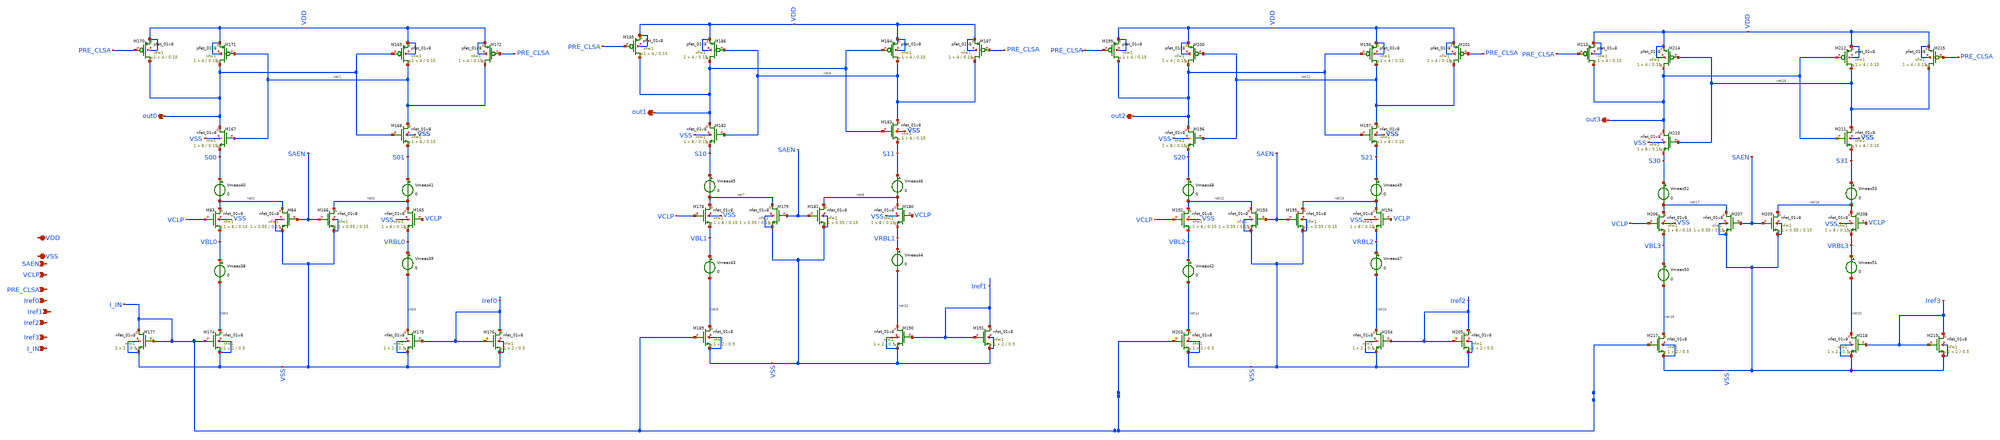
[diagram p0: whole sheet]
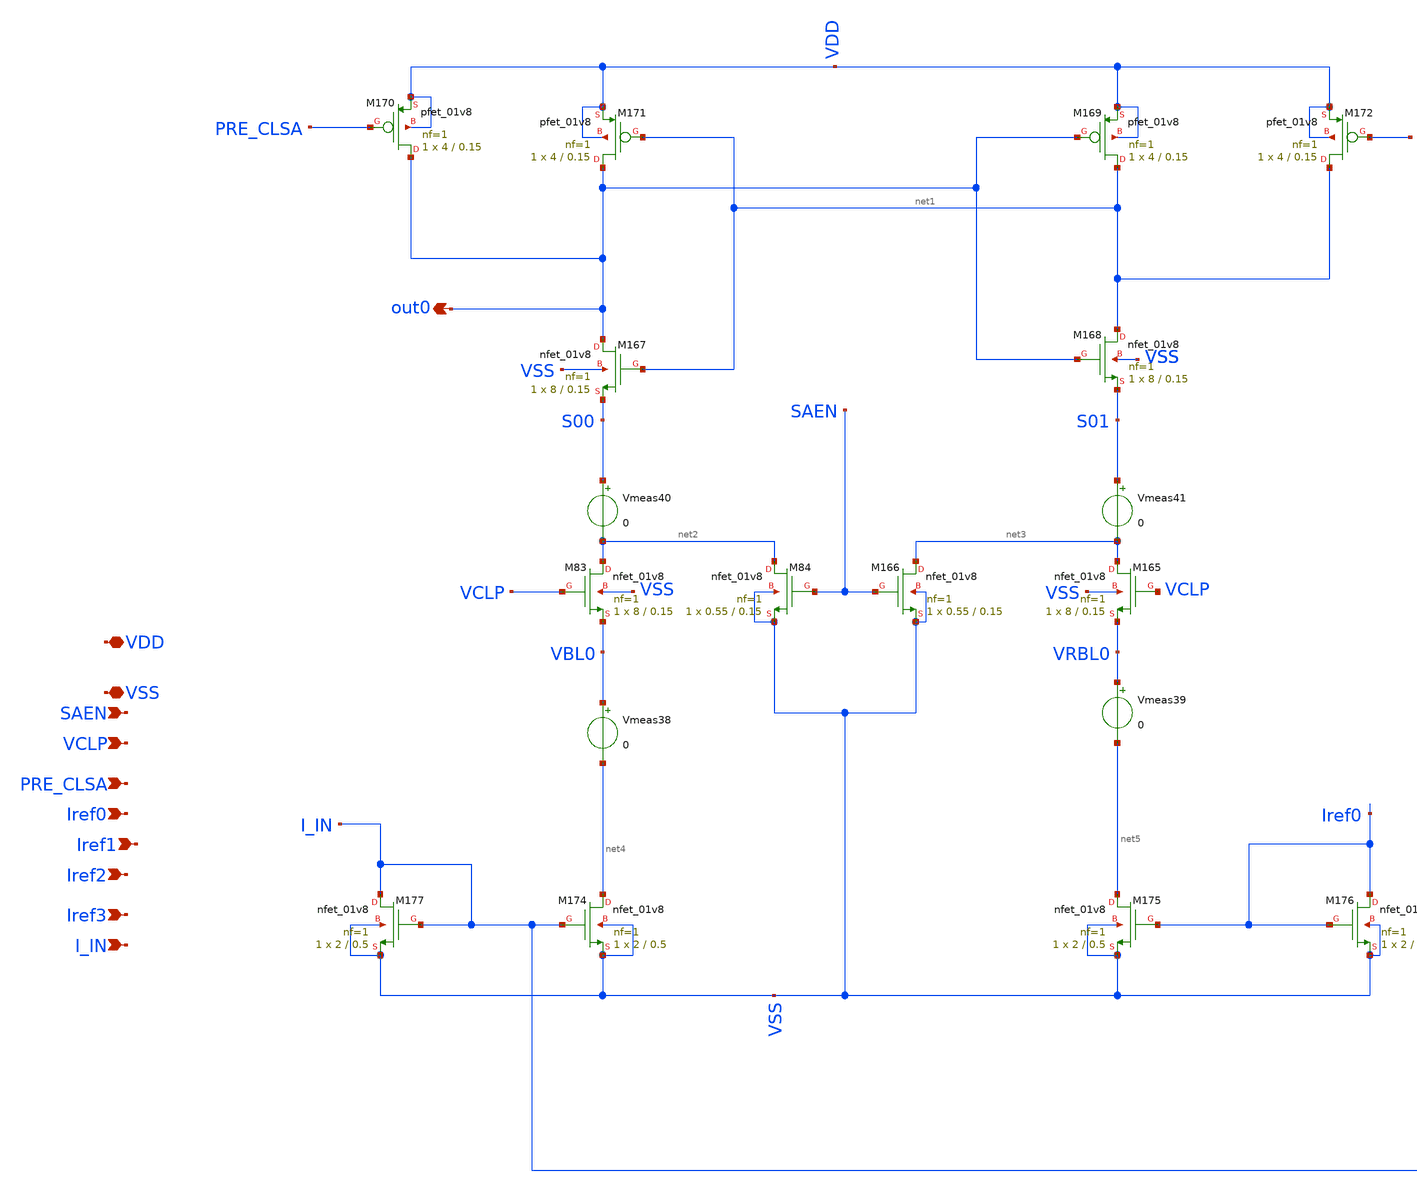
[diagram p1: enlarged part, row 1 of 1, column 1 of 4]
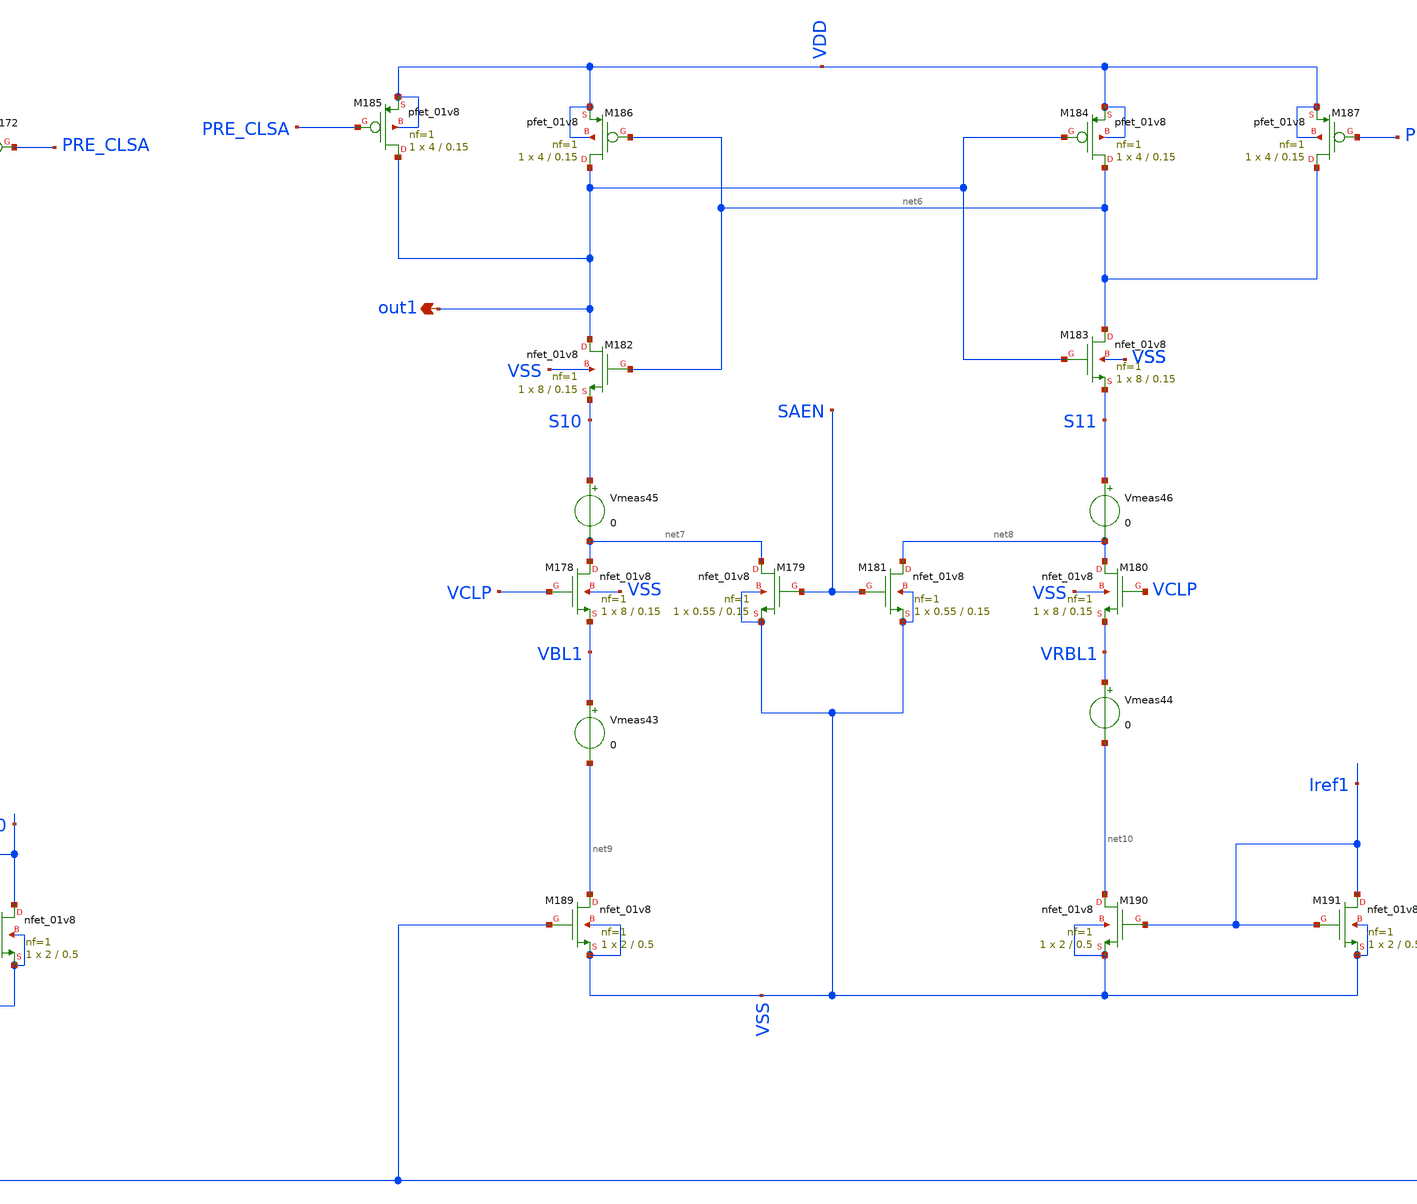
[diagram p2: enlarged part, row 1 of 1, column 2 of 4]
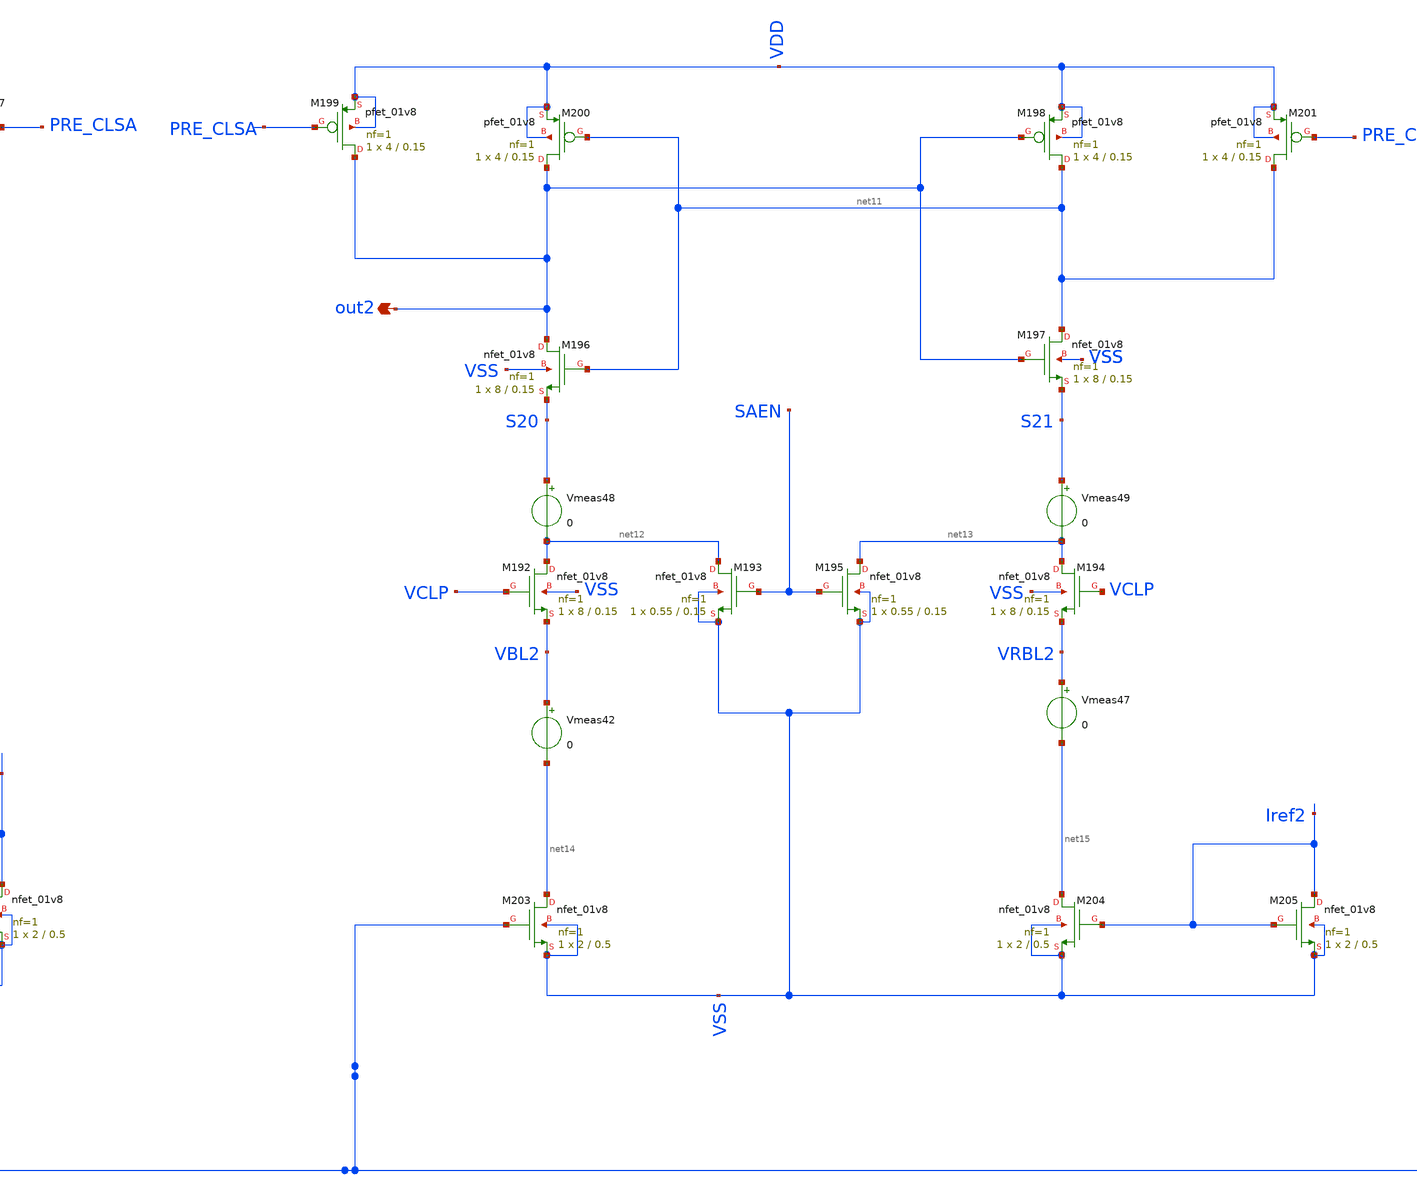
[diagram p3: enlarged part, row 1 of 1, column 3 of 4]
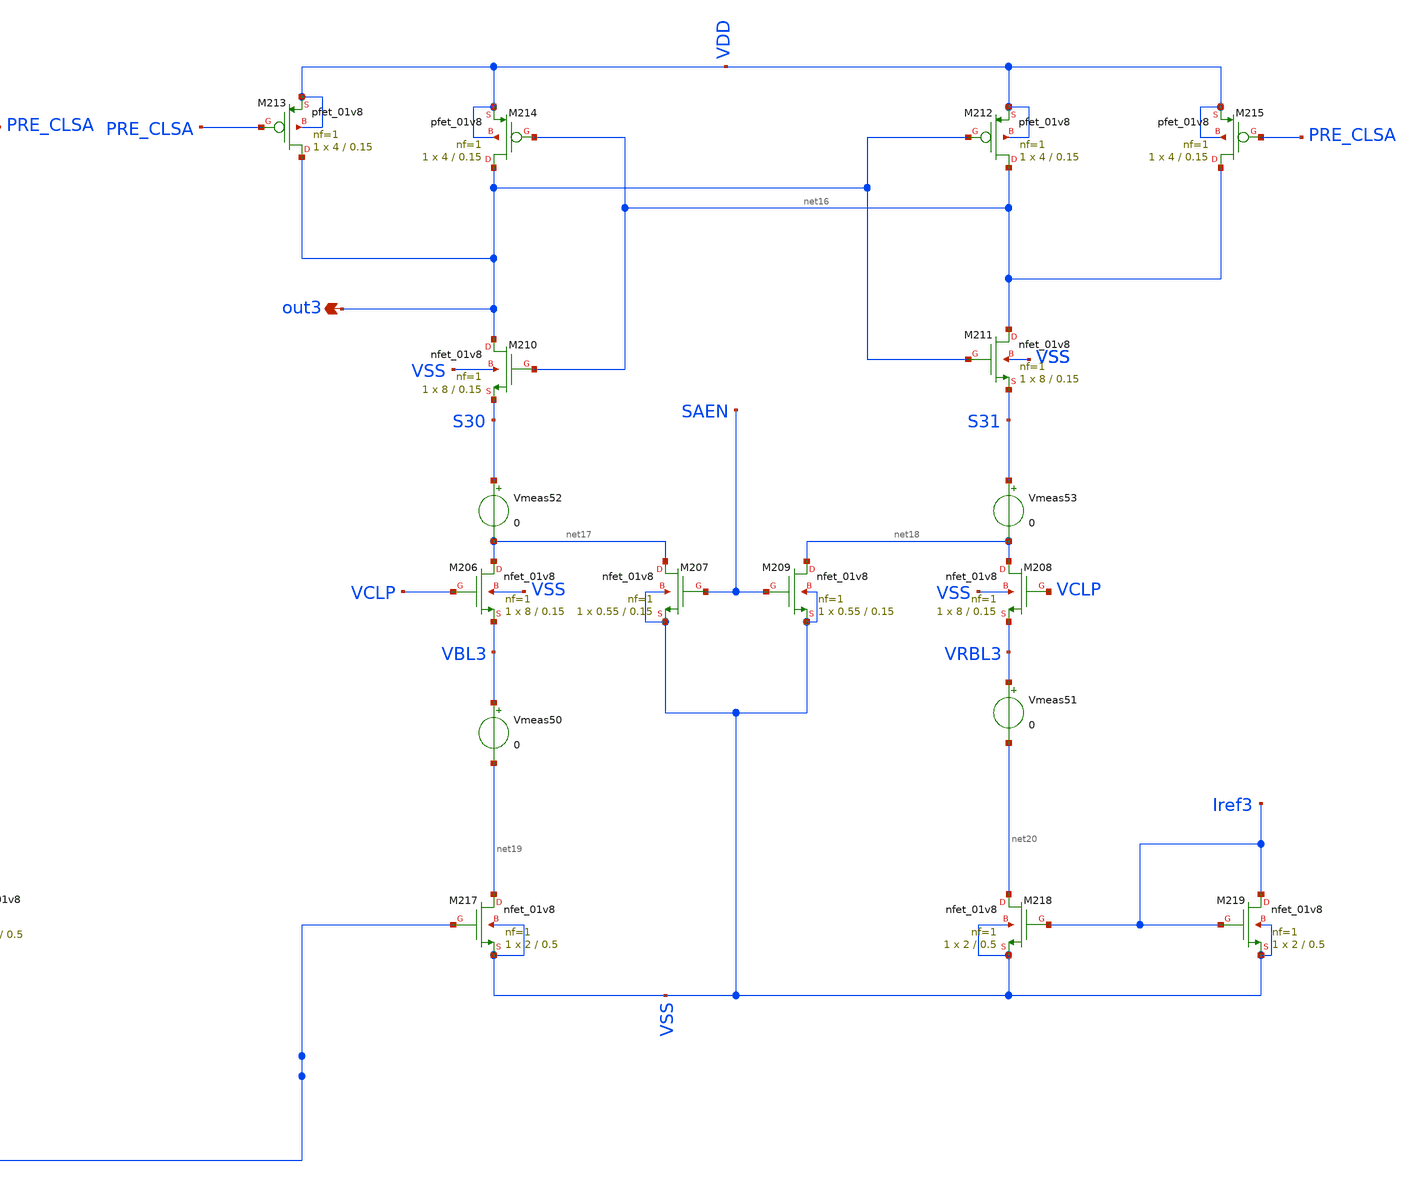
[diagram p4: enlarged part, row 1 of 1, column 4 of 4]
** sch_path: xschem/Integrated_bitcell/ADC_CLSA_4.sch
**.subckt ADC_CLSA_4 out0 out1 out2 out3 VDD VSS VCLP PRE_CLSA Iref0 Iref1 Iref2 Iref3 SAEN I_IN
*.opin out0
*.opin out1
*.opin out2
*.opin out3
*.iopin VDD
*.iopin VSS
*.ipin VCLP
*.ipin PRE_CLSA
*.ipin Iref0
*.ipin Iref1
*.ipin Iref2
*.ipin Iref3
*.ipin SAEN
*.ipin I_IN
XM83 net2 VCLP VBL0 VSS sky130_fd_pr__nfet_01v8 L=0.15 W=8 nf=1 ad='int((nf+1)/2) * W/nf * 0.29' as='int((nf+2)/2) * W/nf * 0.29'
+ pd='2*int((nf+1)/2) * (W/nf + 0.29)' ps='2*int((nf+2)/2) * (W/nf + 0.29)' nrd='0.29 / W' nrs='0.29 / W'
+ sa=0 sb=0 sd=0 mult=1 m=1
XM84 net2 SAEN VSS VSS sky130_fd_pr__nfet_01v8 L=0.15 W=0.55 nf=1 ad='int((nf+1)/2) * W/nf * 0.29' as='int((nf+2)/2) * W/nf * 0.29'
+ pd='2*int((nf+1)/2) * (W/nf + 0.29)' ps='2*int((nf+2)/2) * (W/nf + 0.29)' nrd='0.29 / W' nrs='0.29 / W'
+ sa=0 sb=0 sd=0 mult=1 m=1
XM165 net3 VCLP VRBL0 VSS sky130_fd_pr__nfet_01v8 L=0.15 W=8 nf=1 ad='int((nf+1)/2) * W/nf * 0.29' as='int((nf+2)/2) * W/nf * 0.29'
+ pd='2*int((nf+1)/2) * (W/nf + 0.29)' ps='2*int((nf+2)/2) * (W/nf + 0.29)' nrd='0.29 / W' nrs='0.29 / W'
+ sa=0 sb=0 sd=0 mult=1 m=1
XM166 net3 SAEN VSS VSS sky130_fd_pr__nfet_01v8 L=0.15 W=0.55 nf=1 ad='int((nf+1)/2) * W/nf * 0.29' as='int((nf+2)/2) * W/nf * 0.29'
+ pd='2*int((nf+1)/2) * (W/nf + 0.29)' ps='2*int((nf+2)/2) * (W/nf + 0.29)' nrd='0.29 / W' nrs='0.29 / W'
+ sa=0 sb=0 sd=0 mult=1 m=1
XM167 out0 net1 S00 VSS sky130_fd_pr__nfet_01v8 L=0.15 W=8 nf=1 ad='int((nf+1)/2) * W/nf * 0.29' as='int((nf+2)/2) * W/nf * 0.29'
+ pd='2*int((nf+1)/2) * (W/nf + 0.29)' ps='2*int((nf+2)/2) * (W/nf + 0.29)' nrd='0.29 / W' nrs='0.29 / W'
+ sa=0 sb=0 sd=0 mult=1 m=1
XM168 net1 out0 S01 VSS sky130_fd_pr__nfet_01v8 L=0.15 W=8 nf=1 ad='int((nf+1)/2) * W/nf * 0.29' as='int((nf+2)/2) * W/nf * 0.29'
+ pd='2*int((nf+1)/2) * (W/nf + 0.29)' ps='2*int((nf+2)/2) * (W/nf + 0.29)' nrd='0.29 / W' nrs='0.29 / W'
+ sa=0 sb=0 sd=0 mult=1 m=1
XM169 net1 out0 VDD VDD sky130_fd_pr__pfet_01v8 L=0.15 W=4 nf=1 ad='int((nf+1)/2) * W/nf * 0.29' as='int((nf+2)/2) * W/nf * 0.29'
+ pd='2*int((nf+1)/2) * (W/nf + 0.29)' ps='2*int((nf+2)/2) * (W/nf + 0.29)' nrd='0.29 / W' nrs='0.29 / W'
+ sa=0 sb=0 sd=0 mult=1 m=1
XM170 out0 PRE_CLSA VDD VDD sky130_fd_pr__pfet_01v8 L=0.15 W=4 nf=1 ad='int((nf+1)/2) * W/nf * 0.29'
+ as='int((nf+2)/2) * W/nf * 0.29' pd='2*int((nf+1)/2) * (W/nf + 0.29)' ps='2*int((nf+2)/2) * (W/nf + 0.29)'
+ nrd='0.29 / W' nrs='0.29 / W' sa=0 sb=0 sd=0 mult=1 m=1
XM171 out0 net1 VDD VDD sky130_fd_pr__pfet_01v8 L=0.15 W=4 nf=1 ad='int((nf+1)/2) * W/nf * 0.29' as='int((nf+2)/2) * W/nf * 0.29'
+ pd='2*int((nf+1)/2) * (W/nf + 0.29)' ps='2*int((nf+2)/2) * (W/nf + 0.29)' nrd='0.29 / W' nrs='0.29 / W'
+ sa=0 sb=0 sd=0 mult=1 m=1
XM172 net1 PRE_CLSA VDD VDD sky130_fd_pr__pfet_01v8 L=0.15 W=4 nf=1 ad='int((nf+1)/2) * W/nf * 0.29'
+ as='int((nf+2)/2) * W/nf * 0.29' pd='2*int((nf+1)/2) * (W/nf + 0.29)' ps='2*int((nf+2)/2) * (W/nf + 0.29)'
+ nrd='0.29 / W' nrs='0.29 / W' sa=0 sb=0 sd=0 mult=1 m=1
Vmeas38 VBL0 net4 0
Vmeas39 VRBL0 net5 0
XM174 net4 I_IN VSS VSS sky130_fd_pr__nfet_01v8 L=0.5 W=2 nf=1 ad='int((nf+1)/2) * W/nf * 0.29' as='int((nf+2)/2) * W/nf * 0.29'
+ pd='2*int((nf+1)/2) * (W/nf + 0.29)' ps='2*int((nf+2)/2) * (W/nf + 0.29)' nrd='0.29 / W' nrs='0.29 / W'
+ sa=0 sb=0 sd=0 mult=1 m=1
XM175 net5 Iref0 VSS VSS sky130_fd_pr__nfet_01v8 L=0.5 W=2 nf=1 ad='int((nf+1)/2) * W/nf * 0.29' as='int((nf+2)/2) * W/nf * 0.29'
+ pd='2*int((nf+1)/2) * (W/nf + 0.29)' ps='2*int((nf+2)/2) * (W/nf + 0.29)' nrd='0.29 / W' nrs='0.29 / W'
+ sa=0 sb=0 sd=0 mult=1 m=1
XM176 Iref0 Iref0 VSS VSS sky130_fd_pr__nfet_01v8 L=0.5 W=2 nf=1 ad='int((nf+1)/2) * W/nf * 0.29' as='int((nf+2)/2) * W/nf * 0.29'
+ pd='2*int((nf+1)/2) * (W/nf + 0.29)' ps='2*int((nf+2)/2) * (W/nf + 0.29)' nrd='0.29 / W' nrs='0.29 / W'
+ sa=0 sb=0 sd=0 mult=1 m=1
XM177 I_IN I_IN VSS VSS sky130_fd_pr__nfet_01v8 L=0.5 W=2 nf=1 ad='int((nf+1)/2) * W/nf * 0.29' as='int((nf+2)/2) * W/nf * 0.29'
+ pd='2*int((nf+1)/2) * (W/nf + 0.29)' ps='2*int((nf+2)/2) * (W/nf + 0.29)' nrd='0.29 / W' nrs='0.29 / W'
+ sa=0 sb=0 sd=0 mult=1 m=1
Vmeas40 S00 net2 0
Vmeas41 S01 net3 0
XM178 net7 VCLP VBL1 VSS sky130_fd_pr__nfet_01v8 L=0.15 W=8 nf=1 ad='int((nf+1)/2) * W/nf * 0.29' as='int((nf+2)/2) * W/nf * 0.29'
+ pd='2*int((nf+1)/2) * (W/nf + 0.29)' ps='2*int((nf+2)/2) * (W/nf + 0.29)' nrd='0.29 / W' nrs='0.29 / W'
+ sa=0 sb=0 sd=0 mult=1 m=1
XM179 net7 SAEN VSS VSS sky130_fd_pr__nfet_01v8 L=0.15 W=0.55 nf=1 ad='int((nf+1)/2) * W/nf * 0.29' as='int((nf+2)/2) * W/nf * 0.29'
+ pd='2*int((nf+1)/2) * (W/nf + 0.29)' ps='2*int((nf+2)/2) * (W/nf + 0.29)' nrd='0.29 / W' nrs='0.29 / W'
+ sa=0 sb=0 sd=0 mult=1 m=1
XM180 net8 VCLP VRBL1 VSS sky130_fd_pr__nfet_01v8 L=0.15 W=8 nf=1 ad='int((nf+1)/2) * W/nf * 0.29' as='int((nf+2)/2) * W/nf * 0.29'
+ pd='2*int((nf+1)/2) * (W/nf + 0.29)' ps='2*int((nf+2)/2) * (W/nf + 0.29)' nrd='0.29 / W' nrs='0.29 / W'
+ sa=0 sb=0 sd=0 mult=1 m=1
XM181 net8 SAEN VSS VSS sky130_fd_pr__nfet_01v8 L=0.15 W=0.55 nf=1 ad='int((nf+1)/2) * W/nf * 0.29' as='int((nf+2)/2) * W/nf * 0.29'
+ pd='2*int((nf+1)/2) * (W/nf + 0.29)' ps='2*int((nf+2)/2) * (W/nf + 0.29)' nrd='0.29 / W' nrs='0.29 / W'
+ sa=0 sb=0 sd=0 mult=1 m=1
XM182 out1 net6 S10 VSS sky130_fd_pr__nfet_01v8 L=0.15 W=8 nf=1 ad='int((nf+1)/2) * W/nf * 0.29' as='int((nf+2)/2) * W/nf * 0.29'
+ pd='2*int((nf+1)/2) * (W/nf + 0.29)' ps='2*int((nf+2)/2) * (W/nf + 0.29)' nrd='0.29 / W' nrs='0.29 / W'
+ sa=0 sb=0 sd=0 mult=1 m=1
XM183 net6 out1 S11 VSS sky130_fd_pr__nfet_01v8 L=0.15 W=8 nf=1 ad='int((nf+1)/2) * W/nf * 0.29' as='int((nf+2)/2) * W/nf * 0.29'
+ pd='2*int((nf+1)/2) * (W/nf + 0.29)' ps='2*int((nf+2)/2) * (W/nf + 0.29)' nrd='0.29 / W' nrs='0.29 / W'
+ sa=0 sb=0 sd=0 mult=1 m=1
XM184 net6 out1 VDD VDD sky130_fd_pr__pfet_01v8 L=0.15 W=4 nf=1 ad='int((nf+1)/2) * W/nf * 0.29' as='int((nf+2)/2) * W/nf * 0.29'
+ pd='2*int((nf+1)/2) * (W/nf + 0.29)' ps='2*int((nf+2)/2) * (W/nf + 0.29)' nrd='0.29 / W' nrs='0.29 / W'
+ sa=0 sb=0 sd=0 mult=1 m=1
XM185 out1 PRE_CLSA VDD VDD sky130_fd_pr__pfet_01v8 L=0.15 W=4 nf=1 ad='int((nf+1)/2) * W/nf * 0.29'
+ as='int((nf+2)/2) * W/nf * 0.29' pd='2*int((nf+1)/2) * (W/nf + 0.29)' ps='2*int((nf+2)/2) * (W/nf + 0.29)'
+ nrd='0.29 / W' nrs='0.29 / W' sa=0 sb=0 sd=0 mult=1 m=1
XM186 out1 net6 VDD VDD sky130_fd_pr__pfet_01v8 L=0.15 W=4 nf=1 ad='int((nf+1)/2) * W/nf * 0.29' as='int((nf+2)/2) * W/nf * 0.29'
+ pd='2*int((nf+1)/2) * (W/nf + 0.29)' ps='2*int((nf+2)/2) * (W/nf + 0.29)' nrd='0.29 / W' nrs='0.29 / W'
+ sa=0 sb=0 sd=0 mult=1 m=1
XM187 net6 PRE_CLSA VDD VDD sky130_fd_pr__pfet_01v8 L=0.15 W=4 nf=1 ad='int((nf+1)/2) * W/nf * 0.29'
+ as='int((nf+2)/2) * W/nf * 0.29' pd='2*int((nf+1)/2) * (W/nf + 0.29)' ps='2*int((nf+2)/2) * (W/nf + 0.29)'
+ nrd='0.29 / W' nrs='0.29 / W' sa=0 sb=0 sd=0 mult=1 m=1
Vmeas43 VBL1 net9 0
Vmeas44 VRBL1 net10 0
XM189 net9 I_IN VSS VSS sky130_fd_pr__nfet_01v8 L=0.5 W=2 nf=1 ad='int((nf+1)/2) * W/nf * 0.29' as='int((nf+2)/2) * W/nf * 0.29'
+ pd='2*int((nf+1)/2) * (W/nf + 0.29)' ps='2*int((nf+2)/2) * (W/nf + 0.29)' nrd='0.29 / W' nrs='0.29 / W'
+ sa=0 sb=0 sd=0 mult=1 m=1
XM190 net10 Iref1 VSS VSS sky130_fd_pr__nfet_01v8 L=0.5 W=2 nf=1 ad='int((nf+1)/2) * W/nf * 0.29' as='int((nf+2)/2) * W/nf * 0.29'
+ pd='2*int((nf+1)/2) * (W/nf + 0.29)' ps='2*int((nf+2)/2) * (W/nf + 0.29)' nrd='0.29 / W' nrs='0.29 / W'
+ sa=0 sb=0 sd=0 mult=1 m=1
XM191 Iref1 Iref1 VSS VSS sky130_fd_pr__nfet_01v8 L=0.5 W=2 nf=1 ad='int((nf+1)/2) * W/nf * 0.29' as='int((nf+2)/2) * W/nf * 0.29'
+ pd='2*int((nf+1)/2) * (W/nf + 0.29)' ps='2*int((nf+2)/2) * (W/nf + 0.29)' nrd='0.29 / W' nrs='0.29 / W'
+ sa=0 sb=0 sd=0 mult=1 m=1
Vmeas45 S10 net7 0
Vmeas46 S11 net8 0
XM192 net12 VCLP VBL2 VSS sky130_fd_pr__nfet_01v8 L=0.15 W=8 nf=1 ad='int((nf+1)/2) * W/nf * 0.29' as='int((nf+2)/2) * W/nf * 0.29'
+ pd='2*int((nf+1)/2) * (W/nf + 0.29)' ps='2*int((nf+2)/2) * (W/nf + 0.29)' nrd='0.29 / W' nrs='0.29 / W'
+ sa=0 sb=0 sd=0 mult=1 m=1
XM193 net12 SAEN VSS VSS sky130_fd_pr__nfet_01v8 L=0.15 W=0.55 nf=1 ad='int((nf+1)/2) * W/nf * 0.29'
+ as='int((nf+2)/2) * W/nf * 0.29' pd='2*int((nf+1)/2) * (W/nf + 0.29)' ps='2*int((nf+2)/2) * (W/nf + 0.29)'
+ nrd='0.29 / W' nrs='0.29 / W' sa=0 sb=0 sd=0 mult=1 m=1
XM194 net13 VCLP VRBL2 VSS sky130_fd_pr__nfet_01v8 L=0.15 W=8 nf=1 ad='int((nf+1)/2) * W/nf * 0.29' as='int((nf+2)/2) * W/nf * 0.29'
+ pd='2*int((nf+1)/2) * (W/nf + 0.29)' ps='2*int((nf+2)/2) * (W/nf + 0.29)' nrd='0.29 / W' nrs='0.29 / W'
+ sa=0 sb=0 sd=0 mult=1 m=1
XM195 net13 SAEN VSS VSS sky130_fd_pr__nfet_01v8 L=0.15 W=0.55 nf=1 ad='int((nf+1)/2) * W/nf * 0.29'
+ as='int((nf+2)/2) * W/nf * 0.29' pd='2*int((nf+1)/2) * (W/nf + 0.29)' ps='2*int((nf+2)/2) * (W/nf + 0.29)'
+ nrd='0.29 / W' nrs='0.29 / W' sa=0 sb=0 sd=0 mult=1 m=1
XM196 out2 net11 S20 VSS sky130_fd_pr__nfet_01v8 L=0.15 W=8 nf=1 ad='int((nf+1)/2) * W/nf * 0.29' as='int((nf+2)/2) * W/nf * 0.29'
+ pd='2*int((nf+1)/2) * (W/nf + 0.29)' ps='2*int((nf+2)/2) * (W/nf + 0.29)' nrd='0.29 / W' nrs='0.29 / W'
+ sa=0 sb=0 sd=0 mult=1 m=1
XM197 net11 out2 S21 VSS sky130_fd_pr__nfet_01v8 L=0.15 W=8 nf=1 ad='int((nf+1)/2) * W/nf * 0.29' as='int((nf+2)/2) * W/nf * 0.29'
+ pd='2*int((nf+1)/2) * (W/nf + 0.29)' ps='2*int((nf+2)/2) * (W/nf + 0.29)' nrd='0.29 / W' nrs='0.29 / W'
+ sa=0 sb=0 sd=0 mult=1 m=1
XM198 net11 out2 VDD VDD sky130_fd_pr__pfet_01v8 L=0.15 W=4 nf=1 ad='int((nf+1)/2) * W/nf * 0.29' as='int((nf+2)/2) * W/nf * 0.29'
+ pd='2*int((nf+1)/2) * (W/nf + 0.29)' ps='2*int((nf+2)/2) * (W/nf + 0.29)' nrd='0.29 / W' nrs='0.29 / W'
+ sa=0 sb=0 sd=0 mult=1 m=1
XM199 out2 PRE_CLSA VDD VDD sky130_fd_pr__pfet_01v8 L=0.15 W=4 nf=1 ad='int((nf+1)/2) * W/nf * 0.29'
+ as='int((nf+2)/2) * W/nf * 0.29' pd='2*int((nf+1)/2) * (W/nf + 0.29)' ps='2*int((nf+2)/2) * (W/nf + 0.29)'
+ nrd='0.29 / W' nrs='0.29 / W' sa=0 sb=0 sd=0 mult=1 m=1
XM200 out2 net11 VDD VDD sky130_fd_pr__pfet_01v8 L=0.15 W=4 nf=1 ad='int((nf+1)/2) * W/nf * 0.29' as='int((nf+2)/2) * W/nf * 0.29'
+ pd='2*int((nf+1)/2) * (W/nf + 0.29)' ps='2*int((nf+2)/2) * (W/nf + 0.29)' nrd='0.29 / W' nrs='0.29 / W'
+ sa=0 sb=0 sd=0 mult=1 m=1
XM201 net11 PRE_CLSA VDD VDD sky130_fd_pr__pfet_01v8 L=0.15 W=4 nf=1 ad='int((nf+1)/2) * W/nf * 0.29'
+ as='int((nf+2)/2) * W/nf * 0.29' pd='2*int((nf+1)/2) * (W/nf + 0.29)' ps='2*int((nf+2)/2) * (W/nf + 0.29)'
+ nrd='0.29 / W' nrs='0.29 / W' sa=0 sb=0 sd=0 mult=1 m=1
Vmeas42 VBL2 net14 0
Vmeas47 VRBL2 net15 0
XM203 net14 I_IN VSS VSS sky130_fd_pr__nfet_01v8 L=0.5 W=2 nf=1 ad='int((nf+1)/2) * W/nf * 0.29' as='int((nf+2)/2) * W/nf * 0.29'
+ pd='2*int((nf+1)/2) * (W/nf + 0.29)' ps='2*int((nf+2)/2) * (W/nf + 0.29)' nrd='0.29 / W' nrs='0.29 / W'
+ sa=0 sb=0 sd=0 mult=1 m=1
XM204 net15 Iref2 VSS VSS sky130_fd_pr__nfet_01v8 L=0.5 W=2 nf=1 ad='int((nf+1)/2) * W/nf * 0.29' as='int((nf+2)/2) * W/nf * 0.29'
+ pd='2*int((nf+1)/2) * (W/nf + 0.29)' ps='2*int((nf+2)/2) * (W/nf + 0.29)' nrd='0.29 / W' nrs='0.29 / W'
+ sa=0 sb=0 sd=0 mult=1 m=1
XM205 Iref2 Iref2 VSS VSS sky130_fd_pr__nfet_01v8 L=0.5 W=2 nf=1 ad='int((nf+1)/2) * W/nf * 0.29' as='int((nf+2)/2) * W/nf * 0.29'
+ pd='2*int((nf+1)/2) * (W/nf + 0.29)' ps='2*int((nf+2)/2) * (W/nf + 0.29)' nrd='0.29 / W' nrs='0.29 / W'
+ sa=0 sb=0 sd=0 mult=1 m=1
Vmeas48 S20 net12 0
Vmeas49 S21 net13 0
XM206 net17 VCLP VBL3 VSS sky130_fd_pr__nfet_01v8 L=0.15 W=8 nf=1 ad='int((nf+1)/2) * W/nf * 0.29' as='int((nf+2)/2) * W/nf * 0.29'
+ pd='2*int((nf+1)/2) * (W/nf + 0.29)' ps='2*int((nf+2)/2) * (W/nf + 0.29)' nrd='0.29 / W' nrs='0.29 / W'
+ sa=0 sb=0 sd=0 mult=1 m=1
XM207 net17 SAEN VSS VSS sky130_fd_pr__nfet_01v8 L=0.15 W=0.55 nf=1 ad='int((nf+1)/2) * W/nf * 0.29'
+ as='int((nf+2)/2) * W/nf * 0.29' pd='2*int((nf+1)/2) * (W/nf + 0.29)' ps='2*int((nf+2)/2) * (W/nf + 0.29)'
+ nrd='0.29 / W' nrs='0.29 / W' sa=0 sb=0 sd=0 mult=1 m=1
XM208 net18 VCLP VRBL3 VSS sky130_fd_pr__nfet_01v8 L=0.15 W=8 nf=1 ad='int((nf+1)/2) * W/nf * 0.29' as='int((nf+2)/2) * W/nf * 0.29'
+ pd='2*int((nf+1)/2) * (W/nf + 0.29)' ps='2*int((nf+2)/2) * (W/nf + 0.29)' nrd='0.29 / W' nrs='0.29 / W'
+ sa=0 sb=0 sd=0 mult=1 m=1
XM209 net18 SAEN VSS VSS sky130_fd_pr__nfet_01v8 L=0.15 W=0.55 nf=1 ad='int((nf+1)/2) * W/nf * 0.29'
+ as='int((nf+2)/2) * W/nf * 0.29' pd='2*int((nf+1)/2) * (W/nf + 0.29)' ps='2*int((nf+2)/2) * (W/nf + 0.29)'
+ nrd='0.29 / W' nrs='0.29 / W' sa=0 sb=0 sd=0 mult=1 m=1
XM210 out3 net16 S30 VSS sky130_fd_pr__nfet_01v8 L=0.15 W=8 nf=1 ad='int((nf+1)/2) * W/nf * 0.29' as='int((nf+2)/2) * W/nf * 0.29'
+ pd='2*int((nf+1)/2) * (W/nf + 0.29)' ps='2*int((nf+2)/2) * (W/nf + 0.29)' nrd='0.29 / W' nrs='0.29 / W'
+ sa=0 sb=0 sd=0 mult=1 m=1
XM211 net16 out3 S31 VSS sky130_fd_pr__nfet_01v8 L=0.15 W=8 nf=1 ad='int((nf+1)/2) * W/nf * 0.29' as='int((nf+2)/2) * W/nf * 0.29'
+ pd='2*int((nf+1)/2) * (W/nf + 0.29)' ps='2*int((nf+2)/2) * (W/nf + 0.29)' nrd='0.29 / W' nrs='0.29 / W'
+ sa=0 sb=0 sd=0 mult=1 m=1
XM212 net16 out3 VDD VDD sky130_fd_pr__pfet_01v8 L=0.15 W=4 nf=1 ad='int((nf+1)/2) * W/nf * 0.29' as='int((nf+2)/2) * W/nf * 0.29'
+ pd='2*int((nf+1)/2) * (W/nf + 0.29)' ps='2*int((nf+2)/2) * (W/nf + 0.29)' nrd='0.29 / W' nrs='0.29 / W'
+ sa=0 sb=0 sd=0 mult=1 m=1
XM213 out3 PRE_CLSA VDD VDD sky130_fd_pr__pfet_01v8 L=0.15 W=4 nf=1 ad='int((nf+1)/2) * W/nf * 0.29'
+ as='int((nf+2)/2) * W/nf * 0.29' pd='2*int((nf+1)/2) * (W/nf + 0.29)' ps='2*int((nf+2)/2) * (W/nf + 0.29)'
+ nrd='0.29 / W' nrs='0.29 / W' sa=0 sb=0 sd=0 mult=1 m=1
XM214 out3 net16 VDD VDD sky130_fd_pr__pfet_01v8 L=0.15 W=4 nf=1 ad='int((nf+1)/2) * W/nf * 0.29' as='int((nf+2)/2) * W/nf * 0.29'
+ pd='2*int((nf+1)/2) * (W/nf + 0.29)' ps='2*int((nf+2)/2) * (W/nf + 0.29)' nrd='0.29 / W' nrs='0.29 / W'
+ sa=0 sb=0 sd=0 mult=1 m=1
XM215 net16 PRE_CLSA VDD VDD sky130_fd_pr__pfet_01v8 L=0.15 W=4 nf=1 ad='int((nf+1)/2) * W/nf * 0.29'
+ as='int((nf+2)/2) * W/nf * 0.29' pd='2*int((nf+1)/2) * (W/nf + 0.29)' ps='2*int((nf+2)/2) * (W/nf + 0.29)'
+ nrd='0.29 / W' nrs='0.29 / W' sa=0 sb=0 sd=0 mult=1 m=1
Vmeas50 VBL3 net19 0
Vmeas51 VRBL3 net20 0
XM217 net19 I_IN VSS VSS sky130_fd_pr__nfet_01v8 L=0.5 W=2 nf=1 ad='int((nf+1)/2) * W/nf * 0.29' as='int((nf+2)/2) * W/nf * 0.29'
+ pd='2*int((nf+1)/2) * (W/nf + 0.29)' ps='2*int((nf+2)/2) * (W/nf + 0.29)' nrd='0.29 / W' nrs='0.29 / W'
+ sa=0 sb=0 sd=0 mult=1 m=1
XM218 net20 Iref3 VSS VSS sky130_fd_pr__nfet_01v8 L=0.5 W=2 nf=1 ad='int((nf+1)/2) * W/nf * 0.29' as='int((nf+2)/2) * W/nf * 0.29'
+ pd='2*int((nf+1)/2) * (W/nf + 0.29)' ps='2*int((nf+2)/2) * (W/nf + 0.29)' nrd='0.29 / W' nrs='0.29 / W'
+ sa=0 sb=0 sd=0 mult=1 m=1
XM219 Iref3 Iref3 VSS VSS sky130_fd_pr__nfet_01v8 L=0.5 W=2 nf=1 ad='int((nf+1)/2) * W/nf * 0.29' as='int((nf+2)/2) * W/nf * 0.29'
+ pd='2*int((nf+1)/2) * (W/nf + 0.29)' ps='2*int((nf+2)/2) * (W/nf + 0.29)' nrd='0.29 / W' nrs='0.29 / W'
+ sa=0 sb=0 sd=0 mult=1 m=1
Vmeas52 S30 net17 0
Vmeas53 S31 net18 0
**.ends
.end
